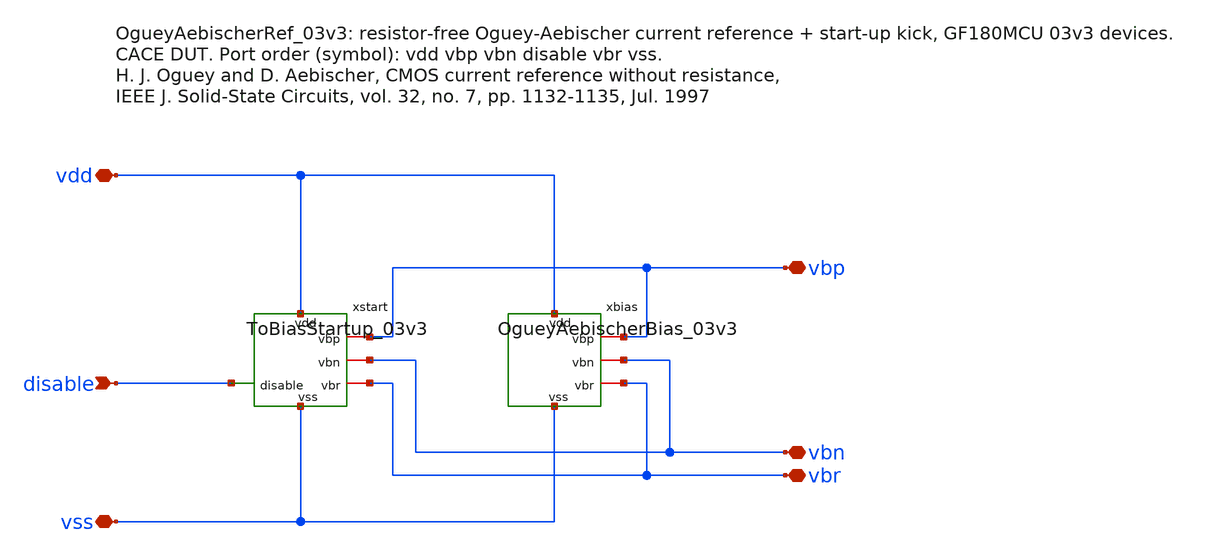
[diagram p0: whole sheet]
** sch_path: macros/OgueyAebischerBias/schematic/xschem/OgueyAebischerRef_03v3.sch
**.subckt OgueyAebischerRef_03v3 vdd vbp vbn disable vbr vss
*.iopin vdd
*.iopin vbp
*.iopin vbn
*.ipin disable
*.iopin vbr
*.iopin vss
xbias vdd vbp vbn vbr vss OgueyAebischerBias_03v3
xstart vdd vbp vbn disable vbr vss ToBiasStartup_03v3
**.ends

* expanding   symbol:  OgueyAebischerBias_03v3.sym # of pins=5
** sym_path: macros/OgueyAebischerBias/schematic/xschem/OgueyAebischerBias_03v3.sym
** sch_path: macros/OgueyAebischerBias/schematic/xschem/OgueyAebischerBias_03v3.sch
.subckt OgueyAebischerBias_03v3 vdd vbp vbn vbr vss
*.iopin vss
*.iopin vdd
*.iopin vbp
*.iopin vbn
*.iopin vbr
XM10 net3 vbn vres vss nfet_03v3 L=2.2u W=88u nf=4 ad='int((nf+1)/2) * W/nf * 0.18u' as='int((nf+2)/2) * W/nf * 0.18u'
+ pd='2*int((nf+1)/2) * (W/nf + 0.18u)' ps='2*int((nf+2)/2) * (W/nf + 0.18u)' nrd='0.18u / W' nrs='0.18u / W'
+ sa=0 sb=0 sd=0 m=1
XM12 vbp vbp vdd vdd pfet_03v3 L=2.8u W=18u nf=1 ad='int((nf+1)/2) * W/nf * 0.18u' as='int((nf+2)/2) * W/nf * 0.18u'
+ pd='2*int((nf+1)/2) * (W/nf + 0.18u)' ps='2*int((nf+2)/2) * (W/nf + 0.18u)' nrd='0.18u / W' nrs='0.18u / W'
+ sa=0 sb=0 sd=0 m=1
XM11 vbn vbn vss vss nfet_03v3 L=2.2u W=22u nf=1 ad='int((nf+1)/2) * W/nf * 0.18u' as='int((nf+2)/2) * W/nf * 0.18u'
+ pd='2*int((nf+1)/2) * (W/nf + 0.18u)' ps='2*int((nf+2)/2) * (W/nf + 0.18u)' nrd='0.18u / W' nrs='0.18u / W'
+ sa=0 sb=0 sd=0 m=1
XM13 net2 vbp vdd vdd pfet_03v3 L=2.8u W=72u nf=4 ad='int((nf+1)/2) * W/nf * 0.18u' as='int((nf+2)/2) * W/nf * 0.18u'
+ pd='2*int((nf+1)/2) * (W/nf + 0.18u)' ps='2*int((nf+2)/2) * (W/nf + 0.18u)' nrd='0.18u / W' nrs='0.18u / W'
+ sa=0 sb=0 sd=0 m=1
XM14 net1 vbp vdd vdd pfet_03v3 L=2.8u W=36u nf=2 ad='int((nf+1)/2) * W/nf * 0.18u' as='int((nf+2)/2) * W/nf * 0.18u'
+ pd='2*int((nf+1)/2) * (W/nf + 0.18u)' ps='2*int((nf+2)/2) * (W/nf + 0.18u)' nrd='0.18u / W' nrs='0.18u / W'
+ sa=0 sb=0 sd=0 m=1
XM16 vres vbr net5 vss nfet_03v3 L=20.4u W=2u nf=1 ad='int((nf+1)/2) * W/nf * 0.18u' as='int((nf+2)/2) * W/nf * 0.18u'
+ pd='2*int((nf+1)/2) * (W/nf + 0.18u)' ps='2*int((nf+2)/2) * (W/nf + 0.18u)' nrd='0.18u / W' nrs='0.18u / W'
+ sa=0 sb=0 sd=0 m=1
XM15 vbr vbr net4 vss nfet_03v3 L=20.4u W=2u nf=1 ad='int((nf+1)/2) * W/nf * 0.18u' as='int((nf+2)/2) * W/nf * 0.18u'
+ pd='2*int((nf+1)/2) * (W/nf + 0.18u)' ps='2*int((nf+2)/2) * (W/nf + 0.18u)' nrd='0.18u / W' nrs='0.18u / W'
+ sa=0 sb=0 sd=0 m=1
Vi1 vbp net3 0
.save i(vi1)
Vi4 net2 vbn 0
.save i(vi4)
Viaux net1 vbr 0
.save i(viaux)
XM18 net5 vbr net6 vss nfet_03v3 L=20.4u W=2u nf=1 ad='int((nf+1)/2) * W/nf * 0.18u' as='int((nf+2)/2) * W/nf * 0.18u'
+ pd='2*int((nf+1)/2) * (W/nf + 0.18u)' ps='2*int((nf+2)/2) * (W/nf + 0.18u)' nrd='0.18u / W' nrs='0.18u / W'
+ sa=0 sb=0 sd=0 m=1
XM17 net4 vbr net7 vss nfet_03v3 L=20.4u W=2u nf=1 ad='int((nf+1)/2) * W/nf * 0.18u' as='int((nf+2)/2) * W/nf * 0.18u'
+ pd='2*int((nf+1)/2) * (W/nf + 0.18u)' ps='2*int((nf+2)/2) * (W/nf + 0.18u)' nrd='0.18u / W' nrs='0.18u / W'
+ sa=0 sb=0 sd=0 m=1
XM20 net6 vbr net9 vss nfet_03v3 L=20.4u W=2u nf=1 ad='int((nf+1)/2) * W/nf * 0.18u' as='int((nf+2)/2) * W/nf * 0.18u'
+ pd='2*int((nf+1)/2) * (W/nf + 0.18u)' ps='2*int((nf+2)/2) * (W/nf + 0.18u)' nrd='0.18u / W' nrs='0.18u / W'
+ sa=0 sb=0 sd=0 m=1
XM19 net7 vbr net8 vss nfet_03v3 L=20.4u W=2u nf=1 ad='int((nf+1)/2) * W/nf * 0.18u' as='int((nf+2)/2) * W/nf * 0.18u'
+ pd='2*int((nf+1)/2) * (W/nf + 0.18u)' ps='2*int((nf+2)/2) * (W/nf + 0.18u)' nrd='0.18u / W' nrs='0.18u / W'
+ sa=0 sb=0 sd=0 m=1
XM22 net9 vbr vss vss nfet_03v3 L=20.4u W=2u nf=1 ad='int((nf+1)/2) * W/nf * 0.18u' as='int((nf+2)/2) * W/nf * 0.18u'
+ pd='2*int((nf+1)/2) * (W/nf + 0.18u)' ps='2*int((nf+2)/2) * (W/nf + 0.18u)' nrd='0.18u / W' nrs='0.18u / W'
+ sa=0 sb=0 sd=0 m=1
XM21 net8 vbr vss vss nfet_03v3 L=20.4u W=2u nf=1 ad='int((nf+1)/2) * W/nf * 0.18u' as='int((nf+2)/2) * W/nf * 0.18u'
+ pd='2*int((nf+1)/2) * (W/nf + 0.18u)' ps='2*int((nf+2)/2) * (W/nf + 0.18u)' nrd='0.18u / W' nrs='0.18u / W'
+ sa=0 sb=0 sd=0 m=1
.ends


* expanding   symbol:  ToBiasStartup_03v3.sym # of pins=6
** sym_path: macros/OgueyAebischerBias/schematic/xschem/ToBiasStartup_03v3.sym
** sch_path: macros/OgueyAebischerBias/schematic/xschem/ToBiasStartup_03v3.sch
.subckt ToBiasStartup_03v3 vdd vbp vbn disable vbr vss
*.iopin vss
*.iopin vdd
*.iopin vbp
*.iopin vbn
*.iopin vbr
*.ipin disable
XM24 vbr disable vss vss nfet_03v3 L=1u W=1u nf=1 ad='int((nf+1)/2) * W/nf * 0.18u' as='int((nf+2)/2) * W/nf * 0.18u'
+ pd='2*int((nf+1)/2) * (W/nf + 0.18u)' ps='2*int((nf+2)/2) * (W/nf + 0.18u)' nrd='0.18u / W' nrs='0.18u / W'
+ sa=0 sb=0 sd=0 m=1
XM22 vbr vkick vdd vdd pfet_03v3 L=1u W=1u nf=1 ad='int((nf+1)/2) * W/nf * 0.18u' as='int((nf+2)/2) * W/nf * 0.18u'
+ pd='2*int((nf+1)/2) * (W/nf + 0.18u)' ps='2*int((nf+2)/2) * (W/nf + 0.18u)' nrd='0.18u / W' nrs='0.18u / W'
+ sa=0 sb=0 sd=0 m=1
XM25 vkick vbp vdd vdd pfet_03v3 L=2.8u W=18u nf=1 ad='int((nf+1)/2) * W/nf * 0.18u' as='int((nf+2)/2) * W/nf * 0.18u'
+ pd='2*int((nf+1)/2) * (W/nf + 0.18u)' ps='2*int((nf+2)/2) * (W/nf + 0.18u)' nrd='0.18u / W' nrs='0.18u / W'
+ sa=0 sb=0 sd=0 m=1
XM23 vbn disable vss vss nfet_03v3 L=1u W=1u nf=1 ad='int((nf+1)/2) * W/nf * 0.18u' as='int((nf+2)/2) * W/nf * 0.18u'
+ pd='2*int((nf+1)/2) * (W/nf + 0.18u)' ps='2*int((nf+2)/2) * (W/nf + 0.18u)' nrd='0.18u / W' nrs='0.18u / W'
+ sa=0 sb=0 sd=0 m=1
XM21 vbn vkick vdd vdd pfet_03v3 L=1u W=1u nf=1 ad='int((nf+1)/2) * W/nf * 0.18u' as='int((nf+2)/2) * W/nf * 0.18u'
+ pd='2*int((nf+1)/2) * (W/nf + 0.18u)' ps='2*int((nf+2)/2) * (W/nf + 0.18u)' nrd='0.18u / W' nrs='0.18u / W'
+ sa=0 sb=0 sd=0 m=1
XM20 disable vkick disable vss nfet_03v3 L=2u W=8u nf=1 ad='int((nf+1)/2) * W/nf * 0.18u' as='int((nf+2)/2) * W/nf * 0.18u'
+ pd='2*int((nf+1)/2) * (W/nf + 0.18u)' ps='2*int((nf+2)/2) * (W/nf + 0.18u)' nrd='0.18u / W' nrs='0.18u / W'
+ sa=0 sb=0 sd=0 m=1
XM26 vdd vbp vdd vss nfet_03v3 L=2u W=8u nf=1 ad='int((nf+1)/2) * W/nf * 0.18u' as='int((nf+2)/2) * W/nf * 0.18u'
+ pd='2*int((nf+1)/2) * (W/nf + 0.18u)' ps='2*int((nf+2)/2) * (W/nf + 0.18u)' nrd='0.18u / W' nrs='0.18u / W'
+ sa=0 sb=0 sd=0 m=1
.ends

.end
